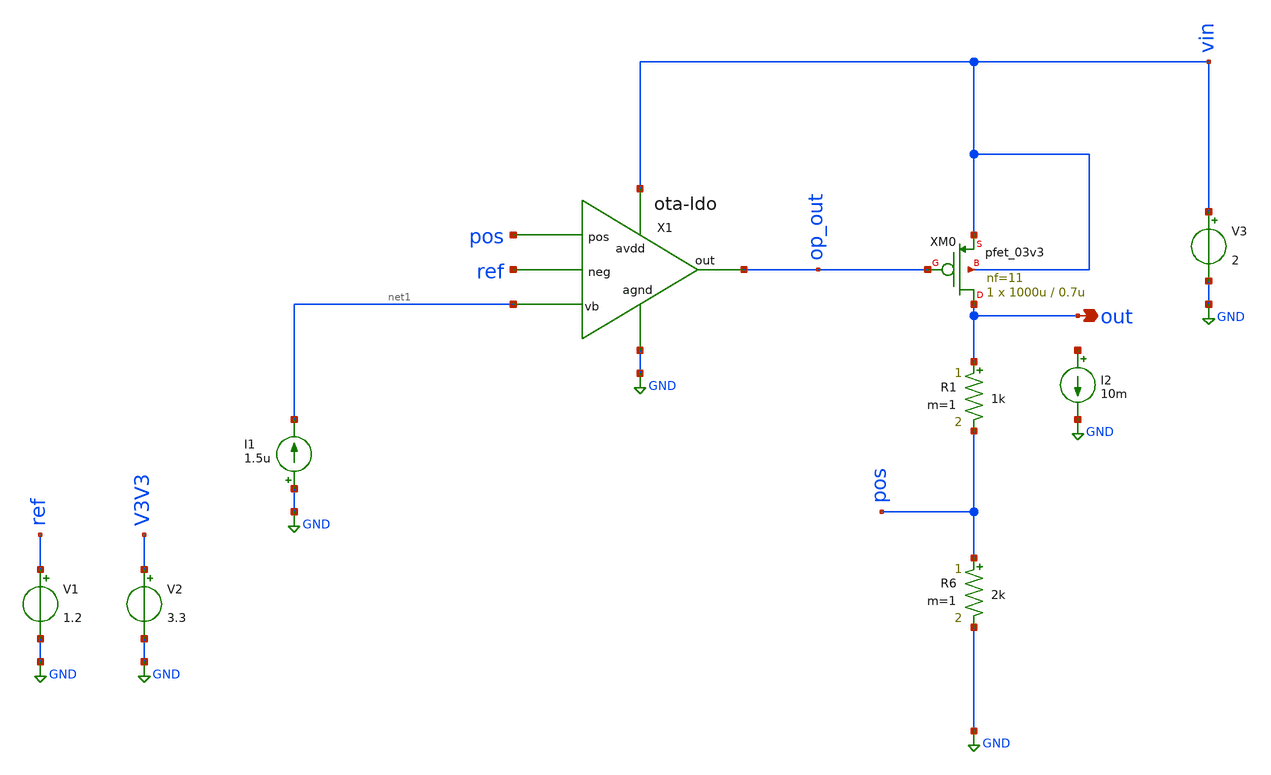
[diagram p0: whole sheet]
** sch_path: LDO/xschem/ldo_gf180.sch
**.subckt ldo_gf180 out
*.opin out
I1 GND net1 1.5u
V1 ref GND 1.2
R1 out pos 1k m=1
R6 pos GND 2k m=1
V2 V3V3 GND 3.3
V3 vin GND 2
X1 vin op_out ref pos net1 GND ota-ldo
XM0 out op_out vin vin pfet_03v3 L=0.7u W=1000u nf=11 ad='int((nf+1)/2) * W/nf * 0.18u' as='int((nf+2)/2) * W/nf * 0.18u'
+ pd='2*int((nf+1)/2) * (W/nf + 0.18u)' ps='2*int((nf+2)/2) * (W/nf + 0.18u)' nrd='0.18u / W' nrs='0.18u / W'
+ sa=0 sb=0 sd=0 m=1
I2 net2 GND 10m
**** begin user architecture code



.include /foss/pdks/gf180mcuC/libs.tech/ngspice/design.ngspice
.lib /foss/pdks/gf180mcuC/libs.tech/ngspice/sm141064.ngspice typical
.lib /foss/pdks/gf180mcuC/libs.tech/ngspice/sm141064.ngspice mimcap_statistical
.lib /foss/pdks/gf180mcuC/libs.tech/ngspice/sm141064.ngspice cap_mim

.param R=36k
*R10 out 0 {R}
IL out 0 PWL(0 0.1m 10u 0.1m 20u 10m 30u 10m)
CL out 0 1p
.options savecurrents

.nodeset v(out)=0
.nodeset v(pos)=0

*TRANSIENT
*.control
*save all
*tran 1ns 2us
*plot v(out) v(ref) v(pos) v(vin)
*plot v(op_out)
*plot v(out)
*plot i(v3)
*plot i(v3)*v(vin)
*.endc

*Stability_Analysis
.control
alter IL 0
alter Vs AC =0
alter Vt AC=1
ac dec 10 1 1G
plot vdb(out)
plot (180/pi)*vp(out)
let ph= (180/pi)*vp(out)
meas ac pm FIND ph WHEN vdb(out)=0
.endc

*SUPPLY SWEEP
*.control
*save all
*dc V3 3.3 0 -0.01
*plot v(out) v(ref) v(pos) v(vin)
*wrdata /foss/designs/LDO_Design/data/data_SuplySweep_Vout.dat v(out)
*wrdata /foss/designs/LDO_Design/data/data_SuplySweep_Vref.dat v(ref)
*wrdata /foss/designs/LDO_Design/data/data_SuplySweep_Vin.dat v(vin)
*plot v(op_out)
*.endc

*PSRR_Analysis
*.control
*save all
*alter V3 AC =1
*ac dec 100 1 1G
*plot vdb(out)
*let gm0=@m.xm0.m0[gm]
*let Zout=(1.5)/(gm0*v(op_out))
*let Zout2=v(out)/gm0
*plot vdb(Zout2)
*wrdata /foss/designs/LDO_Design/data/data_PSRR.dat vdb(out)
*.endc


**Load_Transient
*.control
*alter IL 50u
*alter R10 3600k
*tran 0.1u 100u
*meas TRAN V_ldo_100u FIND v(out) AT=5u
*meas TRAN V_ldo_10m FIND v(out) AT=100u
*let load_reg= V_ldo_100u-V_ldo_10m
*let load_current =(-1*i(V3)-131.8e-6)
*print load_reg
*plot load_current v(out)-1.8
*.endc


**** end user architecture code
**.ends

* expanding   symbol:  ota-ldo.sym # of pins=6
** sym_path: LDO/xschem/ota-ldo/ota-ldo.sym
** sch_path: LDO/xschem/ota-ldo/ota-ldo.sch
.subckt ota-ldo avdd out neg pos vb agnd
*.iopin vb
*.iopin avdd
*.iopin agnd
*.ipin neg
*.ipin pos
*.opin out
XC2 net2 out cap_mim_1f5fF c_width=50e-6 c_length=20e-6 m=1
XM1 net1 neg net3 agnd nfet_03v3 L=0.3u W=10u nf=1 ad='int((nf+1)/2) * W/nf * 0.18u' as='int((nf+2)/2) * W/nf * 0.18u'
+ pd='2*int((nf+1)/2) * (W/nf + 0.18u)' ps='2*int((nf+2)/2) * (W/nf + 0.18u)' nrd='0.18u / W' nrs='0.18u / W'
+ sa=0 sb=0 sd=0 m=1
XM3 net1 net1 avdd avdd pfet_03v3 L=0.8u W=9u nf=1 ad='int((nf+1)/2) * W/nf * 0.18u' as='int((nf+2)/2) * W/nf * 0.18u'
+ pd='2*int((nf+1)/2) * (W/nf + 0.18u)' ps='2*int((nf+2)/2) * (W/nf + 0.18u)' nrd='0.18u / W' nrs='0.18u / W'
+ sa=0 sb=0 sd=0 m=1
XM2 net2 pos net3 agnd nfet_03v3 L=0.3u W=10u nf=1 ad='int((nf+1)/2) * W/nf * 0.18u' as='int((nf+2)/2) * W/nf * 0.18u'
+ pd='2*int((nf+1)/2) * (W/nf + 0.18u)' ps='2*int((nf+2)/2) * (W/nf + 0.18u)' nrd='0.18u / W' nrs='0.18u / W'
+ sa=0 sb=0 sd=0 m=1
XM4 net2 net1 avdd avdd pfet_03v3 L=0.8u W=9u nf=1 ad='int((nf+1)/2) * W/nf * 0.18u' as='int((nf+2)/2) * W/nf * 0.18u'
+ pd='2*int((nf+1)/2) * (W/nf + 0.18u)' ps='2*int((nf+2)/2) * (W/nf + 0.18u)' nrd='0.18u / W' nrs='0.18u / W'
+ sa=0 sb=0 sd=0 m=1
XM7 net3 vb agnd agnd nfet_03v3 L=0.8u W=16u nf=1 ad='int((nf+1)/2) * W/nf * 0.18u' as='int((nf+2)/2) * W/nf * 0.18u'
+ pd='2*int((nf+1)/2) * (W/nf + 0.18u)' ps='2*int((nf+2)/2) * (W/nf + 0.18u)' nrd='0.18u / W' nrs='0.18u / W'
+ sa=0 sb=0 sd=0 m=1
XM8 vb vb agnd agnd nfet_03v3 L=0.8u W=1.66u nf=1 ad='int((nf+1)/2) * W/nf * 0.18u' as='int((nf+2)/2) * W/nf * 0.18u'
+ pd='2*int((nf+1)/2) * (W/nf + 0.18u)' ps='2*int((nf+2)/2) * (W/nf + 0.18u)' nrd='0.18u / W' nrs='0.18u / W'
+ sa=0 sb=0 sd=0 m=1
XM5 out net2 avdd avdd pfet_03v3 L=0.4u W=60u nf=1 ad='int((nf+1)/2) * W/nf * 0.18u' as='int((nf+2)/2) * W/nf * 0.18u'
+ pd='2*int((nf+1)/2) * (W/nf + 0.18u)' ps='2*int((nf+2)/2) * (W/nf + 0.18u)' nrd='0.18u / W' nrs='0.18u / W'
+ sa=0 sb=0 sd=0 m=1
XM6 out vb agnd agnd nfet_03v3 L=0.8u W=60u nf=1 ad='int((nf+1)/2) * W/nf * 0.18u' as='int((nf+2)/2) * W/nf * 0.18u'
+ pd='2*int((nf+1)/2) * (W/nf + 0.18u)' ps='2*int((nf+2)/2) * (W/nf + 0.18u)' nrd='0.18u / W' nrs='0.18u / W'
+ sa=0 sb=0 sd=0 m=1
.ends

.GLOBAL GND
.end
